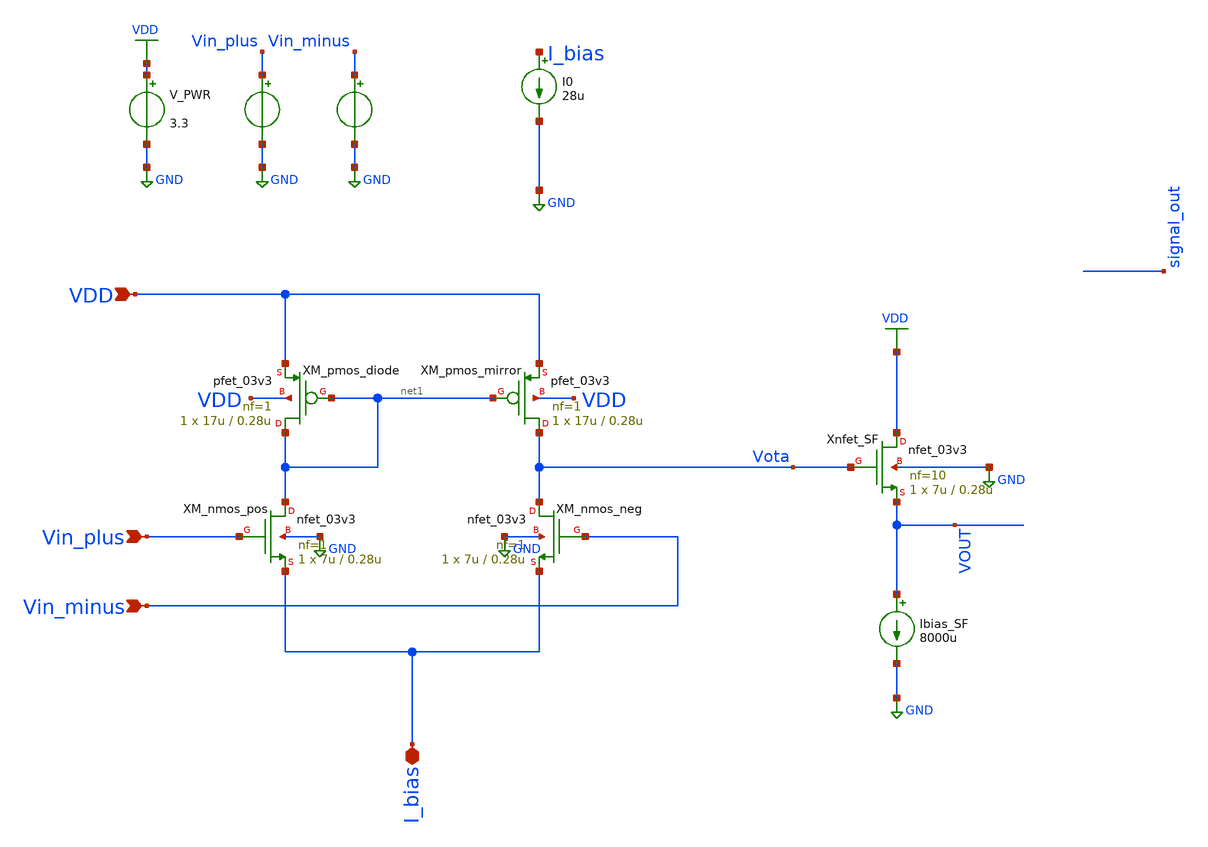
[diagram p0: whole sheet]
** sch_path: src/design_tb/buffer_tb.sch
**.subckt buffer_tb VDD Vin_plus Vin_minus I_bias
*.ipin VDD
*.ipin Vin_plus
*.ipin Vin_minus
*.iopin I_bias
V_PWR VDD GND 3.3
.save i(v_pwr)
Xnfet_SF VDD Vota VOUT GND nfet_03v3 L=0.28u W=7u nf=10 ad='int((nf+1)/2) * W/nf * 0.18u' as='int((nf+2)/2) * W/nf * 0.18u'
+ pd='2*int((nf+1)/2) * (W/nf + 0.18u)' ps='2*int((nf+2)/2) * (W/nf + 0.18u)' nrd='0.18u / W' nrs='0.18u / W'
+ sa=0 sb=0 sd=0 m=1
vrf_plus Vin_plus GND sin( 0.5 0.01 10e6 0 )
.save i(vrf_plus)
XM_nmos_pos net1 Vin_plus I_bias GND nfet_03v3 L=0.28u W=7u nf=1 ad='int((nf+1)/2) * W/nf * 0.18u' as='int((nf+2)/2) * W/nf * 0.18u'
+ pd='2*int((nf+1)/2) * (W/nf + 0.18u)' ps='2*int((nf+2)/2) * (W/nf + 0.18u)' nrd='0.18u / W' nrs='0.18u / W'
+ sa=0 sb=0 sd=0 m=1
XM_nmos_neg Vota Vin_minus I_bias GND nfet_03v3 L=0.28u W=7u nf=1 ad='int((nf+1)/2) * W/nf * 0.18u' as='int((nf+2)/2) * W/nf * 0.18u'
+ pd='2*int((nf+1)/2) * (W/nf + 0.18u)' ps='2*int((nf+2)/2) * (W/nf + 0.18u)' nrd='0.18u / W' nrs='0.18u / W'
+ sa=0 sb=0 sd=0 m=1
XM_pmos_diode net1 net1 VDD VDD pfet_03v3 L=0.28u W=17u nf=1 ad='int((nf+1)/2) * W/nf * 0.18u' as='int((nf+2)/2) * W/nf * 0.18u'
+ pd='2*int((nf+1)/2) * (W/nf + 0.18u)' ps='2*int((nf+2)/2) * (W/nf + 0.18u)' nrd='0.18u / W' nrs='0.18u / W'
+ sa=0 sb=0 sd=0 m=1
XM_pmos_mirror Vota net1 VDD VDD pfet_03v3 L=0.28u W=17u nf=1 ad='int((nf+1)/2) * W/nf * 0.18u' as='int((nf+2)/2) * W/nf * 0.18u'
+ pd='2*int((nf+1)/2) * (W/nf + 0.18u)' ps='2*int((nf+2)/2) * (W/nf + 0.18u)' nrd='0.18u / W' nrs='0.18u / W'
+ sa=0 sb=0 sd=0 m=1
I0 I_bias GND 28u
Ibias_SF VOUT GND 8000u
vrf_minus Vin_minus GND sin( 0.5 0.01 10e6 0 0 180 )
.save i(vrf_minus)
**** begin user architecture code

.include $::180MCU_MODELS/design.ngspice
.lib $::180MCU_MODELS/sm141064.ngspice typical
.lib $::180MCU_MODELS/sm141064.ngspice mimcap_typical
.lib $::180MCU_MODELS/sm141064.ngspice cap_mim
.lib $::180MCU_MODELS/sm141064.ngspice res_typical




* let sets vectors to a plot, while set sets a variable, globally accessible in .control
.tran 100p 200n
.op
.save all

*.control
*  set appendwrite
*  op
*  show
*  let sig = v(signal_out)
*  save all
*  write buffer_tb.raw
*.endc


**** end user architecture code
**.ends
.GLOBAL VDD
.GLOBAL GND
.end
